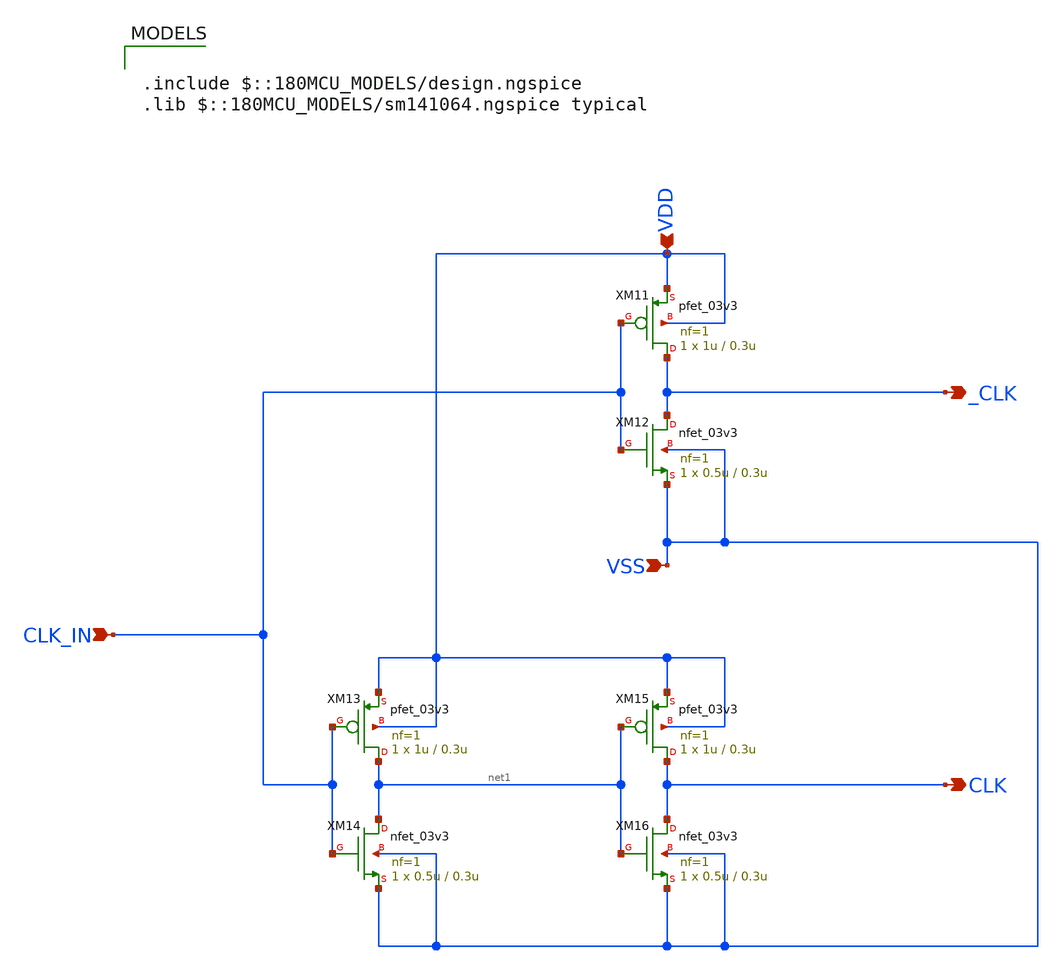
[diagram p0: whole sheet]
** sch_path: ISSCC26/submitted_notebooks/Low Mismatch 4 Channels Instrumentation Amplifier EEG/Complementary Clock and Inverter/Schematic/clk_cs.sch
**.subckt clk_cs CLK _CLK CLK_IN VSS VDD
*.opin CLK
*.opin _CLK
*.ipin CLK_IN
*.ipin VSS
*.ipin VDD
XM11 _CLK CLK_IN VDD VDD pfet_03v3 L=0.3u W=1u nf=1 ad='int((nf+1)/2) * W/nf * 0.18u' as='int((nf+2)/2) * W/nf * 0.18u'
+ pd='2*int((nf+1)/2) * (W/nf + 0.18u)' ps='2*int((nf+2)/2) * (W/nf + 0.18u)' nrd='0.18u / W' nrs='0.18u / W'
+ sa=0 sb=0 sd=0 m=1
XM12 _CLK CLK_IN VSS VSS nfet_03v3 L=0.3u W=0.5u nf=1 ad='int((nf+1)/2) * W/nf * 0.18u' as='int((nf+2)/2) * W/nf * 0.18u'
+ pd='2*int((nf+1)/2) * (W/nf + 0.18u)' ps='2*int((nf+2)/2) * (W/nf + 0.18u)' nrd='0.18u / W' nrs='0.18u / W'
+ sa=0 sb=0 sd=0 m=1
XM13 net1 CLK_IN VDD VDD pfet_03v3 L=0.3u W=1u nf=1 ad='int((nf+1)/2) * W/nf * 0.18u' as='int((nf+2)/2) * W/nf * 0.18u'
+ pd='2*int((nf+1)/2) * (W/nf + 0.18u)' ps='2*int((nf+2)/2) * (W/nf + 0.18u)' nrd='0.18u / W' nrs='0.18u / W'
+ sa=0 sb=0 sd=0 m=1
XM14 net1 CLK_IN VSS VSS nfet_03v3 L=0.3u W=0.5u nf=1 ad='int((nf+1)/2) * W/nf * 0.18u' as='int((nf+2)/2) * W/nf * 0.18u'
+ pd='2*int((nf+1)/2) * (W/nf + 0.18u)' ps='2*int((nf+2)/2) * (W/nf + 0.18u)' nrd='0.18u / W' nrs='0.18u / W'
+ sa=0 sb=0 sd=0 m=1
XM15 CLK net1 VDD VDD pfet_03v3 L=0.3u W=1u nf=1 ad='int((nf+1)/2) * W/nf * 0.18u' as='int((nf+2)/2) * W/nf * 0.18u'
+ pd='2*int((nf+1)/2) * (W/nf + 0.18u)' ps='2*int((nf+2)/2) * (W/nf + 0.18u)' nrd='0.18u / W' nrs='0.18u / W'
+ sa=0 sb=0 sd=0 m=1
XM16 CLK net1 VSS VSS nfet_03v3 L=0.3u W=0.5u nf=1 ad='int((nf+1)/2) * W/nf * 0.18u' as='int((nf+2)/2) * W/nf * 0.18u'
+ pd='2*int((nf+1)/2) * (W/nf + 0.18u)' ps='2*int((nf+2)/2) * (W/nf + 0.18u)' nrd='0.18u / W' nrs='0.18u / W'
+ sa=0 sb=0 sd=0 m=1
**** begin user architecture code

.include $::180MCU_MODELS/design.ngspice
.lib $::180MCU_MODELS/sm141064.ngspice typical

**** end user architecture code
**.ends
.end
